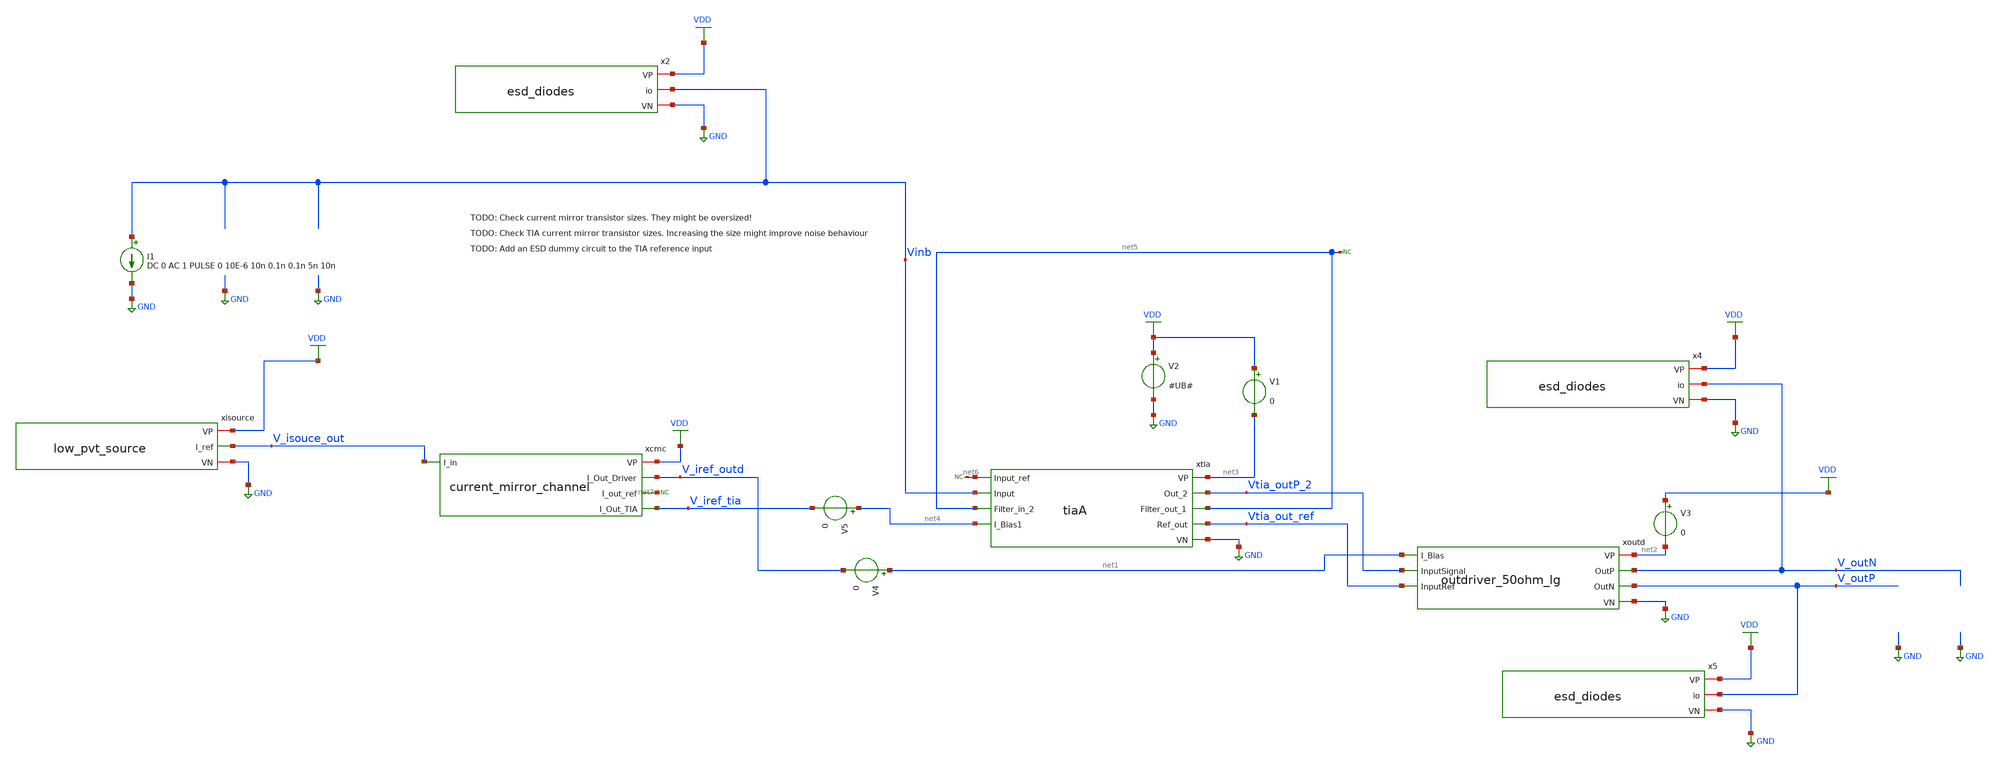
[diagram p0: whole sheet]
** sch_path: xschem/test/test_tia_integration_mc.sch
**.subckt test_tia_integration_mc
xisource VDD V_isouce_out GND low_pvt_source
I1 Vinb GND DC 0 AC 1 PULSE 0 10E-6 10n 0.1n 0.1n 5n 10n
xcmc VDD V_isouce_out V_iref_outd net7 V_iref_tia current_mirror_channel
x4 VDD V_outN GND esd_diodes
x5 VDD V_outP GND esd_diodes
x2 VDD Vinb GND esd_diodes
V2 VDD GND #UB#
V4 net1 V_iref_outd 0
V5 net4 V_iref_tia 0
V1 VDD net3 0
* noconn #net7
V3 VDD net2 0
xtia net3 Vtia_outP_2 net5 net6 Vinb net5 Vtia_out_ref net4 GND tiaA
* noconn #net5
* noconn #net6
xoutd net2 V_outN V_outP net1 Vtia_outP_2 Vtia_out_ref GND outdriver_50ohm_lg
**** begin user architecture code


*.options savecurrents
.option warn=1
* .option temp=100
.control
set wr_vecnames
set wr_singlescale
set hcopydevtype=svg
** TIA

set model="#model#"
let mc_runs=10
let mc_runNo = 1


dowhile mc_runNo <= mc_runs
   	destroy all
	let min_temp=0
	let var_temp = min_temp
	let max_temp=100
	let temp_step=30
	let noise_no=1
	dowhile var_temp <= max_temp
		option temp=$&var_temp
		save all
		op
 		wrdata 'result_op_op_{$&var_temp}deg_{$&mc_runNo}.csv' v(v_outp) v(v_outn) v(Vtia_outP_2) v(Vtia_out_ref)
+ v(v_outp)-v(v_outn)  i(V1) v(V_iref_outd) i(V2) i(V3) i(V4) i(V5) v(vinb)
 		*wrdata 'result_op_detail_{$&var_temp}deg_{$&mc_runNo}.csv' v(xtia.vm24D)
		* v(xtia.vm28D)  v(xoutd.v_da2_P)  v(xoutd.v_da2_N)
		* v(xoutd.v_da2_P)-v(xoutd.v_da2_N) v(xoutd.v_da3_P) v(xoutd.v_da3_N)
		* v(xoutd.v_da3_P)-v(xoutd.v_da3_N) v(v_outp_r)-v(v_outn_r)
		* v(xoutd.v_da2_P) v(xoutd.vm18d)
			* i(v.xtia.v1) i(v.xtia.v2)
		* AC analysis
		save all
		ac dec 10 10 1T

		wrdata 'result_ac_ac_{$&var_temp}deg_{$&mc_runNo}.csv' v(vinb) vdb(Vtia_outP_2)  db(v(v_outp)-v(v_outn))
		wrdata 'result_ac_detail_{$&var_temp}deg_{$&mc_runNo}.csv' db((v(xoutd.V_da2_P)-v(xoutd.V_da2_N))/(v(Vtia_outP_2)-v(Vtia_out_ref)))
+ db((v(xoutd.V_da3_P)-v(xoutd.V_da3_N))/(v(xoutd.V_da2_P)-v(xoutd.V_da2_N)))

		let vout_db=db(v(v_outp)-v(v_outn))
		*let vout_r_db=db(v(v_outp_r)-v(v_outn_r))
		*let dvout=v(v_outp)-v(v_outn)
		* Measure AC at output driver
		meas ac gain_tia FIND vdb(vtia_outp_2) AT=200MEG
		meas ac max_gain_tia max vdb(vtia_outp_2) from=1MEG to=100G
		meas ac min_gain_tia min vdb(vtia_outp_2) from=1MEG to=100MEG
		meas ac min_vinb min v(vinb) from=1MEG to=100G
		let bw_gain_tia=gain_tia-3
		meas ac bandwidth_tia when vdb(vtia_outp_2)=bw_gain_tia fall = LAST
		wrdata result_meas_tia_{$&var_temp}deg_{$&mc_runNo}.csv gain_tia max_gain_tia min_gain_tia bandwidth_tia
+ min_vinb


		* Measure AC at output driver
		meas ac gain_out FIND vout_db AT=10MEG
		meas ac max_gain_out max vout_db from=1MEG to=100G
		*meas ac max_gain_out max vout_db from=1MEG to=100G
		meas ac min_gain_out min vout_db from=1MEG to=100MEG
		*meas ac min_gain_out min vout_db from=1MEG to=100MEG
		let bw_gain_out=gain_out-3
		*let bw_gain_out_n=gain_out_n-3
		meas ac bandwidth_out when vout_db=bw_gain_out fall = LAST
		*meas ac bandwidth_out_r when vout_r_db=bw_gain_out fall = LAST
		*meas ac bandwidth_out_n when vout_db=bw_gain_out_n fall = LAST
		wrdata result_meas_out_{$&var_temp}deg_{$&mc_runNo}.csv gain_out max_gain_out  min_gain_out bandwidth_out


		* noise at TIA
		noise v(vtia_outp_2, vtia_out_ref) i1 dec 10 10 2G
		setplot noise1
		wrdata result_noise_tiaov_{$&var_temp}deg_{$&mc_runNo}.csv inoise_spectrum onoise_spectrum

		noise v(vtia_outp_2, vtia_out_ref) i1 dec 10 1MEG 2G
		setplot noise3
		wrdata result_noise_tiazoom_{$&var_temp}deg_{$&mc_runNo}.csv inoise_spectrum onoise_spectrum

		noise v(v_outp, v_outn) i1 dec 10 10 2G
		setplot noise5
		wrdata result_noise_outov_{$&var_temp}deg_{$&mc_runNo}.csv inoise_spectrum onoise_spectrum

		noise v(v_outp, v_outn) i1 dec 10 1MEG 2G
		setplot noise7
		wrdata result_noise_outzoom_{$&var_temp}deg_{$&mc_runNo}.csv inoise_spectrum onoise_spectrum

		tran 0.1ns 30ns

		wrdata result_tran_tran_{$&var_temp}deg_{$&mc_runNo}.csv v(Vtia_outP_2) v(v_outp)-v(v_outn)

		run
		let var_temp = var_temp + temp_step

	end
	let  mc_runNo = mc_runNo +1
	reset
end



.endc




* .include ../../tia.spice
* .include ../../filter_diff.spice
* .include ../../cmm_sense3.spice

.include tiaA.spice
.include current_mirror_channel.spice
.include low_pvt_source.spice
.include outdriver_50ohm_lg.spice
.include esd_diodes.spice



.lib $::SKYWATER_MODELS/sky130.lib.spice #model#
* .lib $::SKYWATER_MODELS/sky130.lib.spice sf
* .lib $::SKYWATER_MODELS/sky130.lib.spice.ll.red ll

**** end user architecture code
**.ends

* expanding   symbol:  ../bias/low_pvt_source.sym # of pins=3
** sym_path: ../bias/low_pvt_source.sym
** sch_path: ../bias/low_pvt_source.sch
.subckt low_pvt_source VP I_ref VN
*.iopin VP
*.opin I_ref
*.iopin VN
XM1 VM1D VM8D VP VP sky130_fd_pr__pfet_01v8 L=1 W=4 nf=1 ad='int((nf+1)/2) * W/nf * 0.29' as='int((nf+2)/2) * W/nf * 0.29'
+ pd='2*int((nf+1)/2) * (W/nf + 0.29)' ps='2*int((nf+2)/2) * (W/nf + 0.29)' nrd='0.29 / W' nrs='0.29 / W'
+ sa=0 sb=0 sd=0 mult=10 m=10
XM2 VM2D VM2D VN VN sky130_fd_pr__nfet_01v8 L=6 W=4 nf=1 ad='int((nf+1)/2) * W/nf * 0.29' as='int((nf+2)/2) * W/nf * 0.29'
+ pd='2*int((nf+1)/2) * (W/nf + 0.29)' ps='2*int((nf+2)/2) * (W/nf + 0.29)' nrd='0.29 / W' nrs='0.29 / W'
+ sa=0 sb=0 sd=0 mult=30 m=30
XM5 VM9D VM8D VM1D VP sky130_fd_pr__pfet_01v8 L=0.2 W=4 nf=1 ad='int((nf+1)/2) * W/nf * 0.29' as='int((nf+2)/2) * W/nf * 0.29'
+ pd='2*int((nf+1)/2) * (W/nf + 0.29)' ps='2*int((nf+2)/2) * (W/nf + 0.29)' nrd='0.29 / W' nrs='0.29 / W'
+ sa=0 sb=0 sd=0 mult=2 m=2
XM11 VM11D VM2D VM12D VN sky130_fd_pr__nfet_01v8 L=6 W=4 nf=1 ad='int((nf+1)/2) * W/nf * 0.29' as='int((nf+2)/2) * W/nf * 0.29'
+ pd='2*int((nf+1)/2) * (W/nf + 0.29)' ps='2*int((nf+2)/2) * (W/nf + 0.29)' nrd='0.29 / W' nrs='0.29 / W'
+ sa=0 sb=0 sd=0 mult=65 m=65
XM12 VM12D VM12G VN VN sky130_fd_pr__nfet_01v8 L=6 W=4 nf=1 ad='int((nf+1)/2) * W/nf * 0.29' as='int((nf+2)/2) * W/nf * 0.29'
+ pd='2*int((nf+1)/2) * (W/nf + 0.29)' ps='2*int((nf+2)/2) * (W/nf + 0.29)' nrd='0.29 / W' nrs='0.29 / W'
+ sa=0 sb=0 sd=0 mult=2 m=2
XM14 VM14D VM12G VN VN sky130_fd_pr__nfet_01v8 L=6 W=4 nf=1 ad='int((nf+1)/2) * W/nf * 0.29' as='int((nf+2)/2) * W/nf * 0.29'
+ pd='2*int((nf+1)/2) * (W/nf + 0.29)' ps='2*int((nf+2)/2) * (W/nf + 0.29)' nrd='0.29 / W' nrs='0.29 / W'
+ sa=0 sb=0 sd=0 mult=2 m=2
XM16 VM16D VM8D VP VP sky130_fd_pr__pfet_01v8 L=1 W=4 nf=1 ad='int((nf+1)/2) * W/nf * 0.29' as='int((nf+2)/2) * W/nf * 0.29'
+ pd='2*int((nf+1)/2) * (W/nf + 0.29)' ps='2*int((nf+2)/2) * (W/nf + 0.29)' nrd='0.29 / W' nrs='0.29 / W'
+ sa=0 sb=0 sd=0 mult=10 m=10
XM17 VM8D VM8D VM16D VP sky130_fd_pr__pfet_01v8 L=0.2 W=4 nf=1 ad='int((nf+1)/2) * W/nf * 0.29' as='int((nf+2)/2) * W/nf * 0.29'
+ pd='2*int((nf+1)/2) * (W/nf + 0.29)' ps='2*int((nf+2)/2) * (W/nf + 0.29)' nrd='0.29 / W' nrs='0.29 / W'
+ sa=0 sb=0 sd=0 mult=2 m=2
XM18 VM18D VM8D VP VP sky130_fd_pr__pfet_01v8 L=1 W=4 nf=1 ad='int((nf+1)/2) * W/nf * 0.29' as='int((nf+2)/2) * W/nf * 0.29'
+ pd='2*int((nf+1)/2) * (W/nf + 0.29)' ps='2*int((nf+2)/2) * (W/nf + 0.29)' nrd='0.29 / W' nrs='0.29 / W'
+ sa=0 sb=0 sd=0 mult=10*3*2 m=10*3*2
XM19 VM14D VM8D VM18D VP sky130_fd_pr__pfet_01v8 L=0.2 W=4 nf=1 ad='int((nf+1)/2) * W/nf * 0.29' as='int((nf+2)/2) * W/nf * 0.29'
+ pd='2*int((nf+1)/2) * (W/nf + 0.29)' ps='2*int((nf+2)/2) * (W/nf + 0.29)' nrd='0.29 / W' nrs='0.29 / W'
+ sa=0 sb=0 sd=0 mult=2*3*2 m=2*3*2
XM20 VM20D VM8D VP VP sky130_fd_pr__pfet_01v8 L=1 W=4 nf=1 ad='int((nf+1)/2) * W/nf * 0.29' as='int((nf+2)/2) * W/nf * 0.29'
+ pd='2*int((nf+1)/2) * (W/nf + 0.29)' ps='2*int((nf+2)/2) * (W/nf + 0.29)' nrd='0.29 / W' nrs='0.29 / W'
+ sa=0 sb=0 sd=0 mult=10*1*1 m=10*1*1
XM21 VM22D VM8D VM20D VP sky130_fd_pr__pfet_01v8 L=0.2 W=4 nf=1 ad='int((nf+1)/2) * W/nf * 0.29' as='int((nf+2)/2) * W/nf * 0.29'
+ pd='2*int((nf+1)/2) * (W/nf + 0.29)' ps='2*int((nf+2)/2) * (W/nf + 0.29)' nrd='0.29 / W' nrs='0.29 / W'
+ sa=0 sb=0 sd=0 mult=2*1*1 m=2*1*1
XM22 VM22D VM4S VM3D VN sky130_fd_pr__nfet_01v8 L=6 W=4 nf=1 ad='int((nf+1)/2) * W/nf * 0.29' as='int((nf+2)/2) * W/nf * 0.29'
+ pd='2*int((nf+1)/2) * (W/nf + 0.29)' ps='2*int((nf+2)/2) * (W/nf + 0.29)' nrd='0.29 / W' nrs='0.29 / W'
+ sa=0 sb=0 sd=0 mult=20 m=20
XM3 VM3D VM3G VN VN sky130_fd_pr__nfet_01v8 L=6 W=4 nf=1 ad='int((nf+1)/2) * W/nf * 0.29' as='int((nf+2)/2) * W/nf * 0.29'
+ pd='2*int((nf+1)/2) * (W/nf + 0.29)' ps='2*int((nf+2)/2) * (W/nf + 0.29)' nrd='0.29 / W' nrs='0.29 / W'
+ sa=0 sb=0 sd=0 mult=4 m=4
XM13 VP VM14D VM12G VM12G sky130_fd_pr__nfet_01v8_lvt L=0.15 W=4 nf=1 ad='int((nf+1)/2) * W/nf * 0.29'
+ as='int((nf+2)/2) * W/nf * 0.29' pd='2*int((nf+1)/2) * (W/nf + 0.29)' ps='2*int((nf+2)/2) * (W/nf + 0.29)'
+ nrd='0.29 / W' nrs='0.29 / W' sa=0 sb=0 sd=0 mult=20 m=20
XM4 I_ref VM22D VM4S VN sky130_fd_pr__nfet_01v8_lvt L=0.15 W=4 nf=1 ad='int((nf+1)/2) * W/nf * 0.29'
+ as='int((nf+2)/2) * W/nf * 0.29' pd='2*int((nf+1)/2) * (W/nf + 0.29)' ps='2*int((nf+2)/2) * (W/nf + 0.29)'
+ nrd='0.29 / W' nrs='0.29 / W' sa=0 sb=0 sd=0 mult=20 m=20
XM48 VM50D VM11D VP VP sky130_fd_pr__pfet_01v8 L=2 W=0.5 nf=1 ad='int((nf+1)/2) * W/nf * 0.29' as='int((nf+2)/2) * W/nf * 0.29'
+ pd='2*int((nf+1)/2) * (W/nf + 0.29)' ps='2*int((nf+2)/2) * (W/nf + 0.29)' nrd='0.29 / W' nrs='0.29 / W'
+ sa=0 sb=0 sd=0 mult=1 m=1
XM50 VM50D VM11D VN VN sky130_fd_pr__nfet_01v8_lvt L=0.2 W=4 nf=1 ad='int((nf+1)/2) * W/nf * 0.29' as='int((nf+2)/2) * W/nf * 0.29'
+ pd='2*int((nf+1)/2) * (W/nf + 0.29)' ps='2*int((nf+2)/2) * (W/nf + 0.29)' nrd='0.29 / W' nrs='0.29 / W'
+ sa=0 sb=0 sd=0 mult=10 m=10
XC3 VP VM8D sky130_fd_pr__cap_mim_m3_1 W=20 L=20 MF=1 m=1
XM8 VM8D VM9D VM11D VM11D sky130_fd_pr__nfet_01v8_lvt L=1 W=4 nf=1 ad='int((nf+1)/2) * W/nf * 0.29' as='int((nf+2)/2) * W/nf * 0.29'
+ pd='2*int((nf+1)/2) * (W/nf + 0.29)' ps='2*int((nf+2)/2) * (W/nf + 0.29)' nrd='0.29 / W' nrs='0.29 / W'
+ sa=0 sb=0 sd=0 mult=20 m=20
XM9 VM9D VM9D VM2D VM2D sky130_fd_pr__nfet_01v8_lvt L=1 W=4 nf=1 ad='int((nf+1)/2) * W/nf * 0.29' as='int((nf+2)/2) * W/nf * 0.29'
+ pd='2*int((nf+1)/2) * (W/nf + 0.29)' ps='2*int((nf+2)/2) * (W/nf + 0.29)' nrd='0.29 / W' nrs='0.29 / W'
+ sa=0 sb=0 sd=0 mult=20 m=20
XM10 VM8D VM50D VN VN sky130_fd_pr__nfet_01v8 L=2 W=0.5 nf=1 ad='int((nf+1)/2) * W/nf * 0.29' as='int((nf+2)/2) * W/nf * 0.29'
+ pd='2*int((nf+1)/2) * (W/nf + 0.29)' ps='2*int((nf+2)/2) * (W/nf + 0.29)' nrd='0.29 / W' nrs='0.29 / W'
+ sa=0 sb=0 sd=0 mult=1 m=1
XR7 net3 VM4S VN sky130_fd_pr__res_xhigh_po_1p41 L=10 mult=1 m=1
XR3 net4 net3 VN sky130_fd_pr__res_xhigh_po_1p41 L=10 mult=1 m=1
XR4 net2 net4 VN sky130_fd_pr__res_xhigh_po_1p41 L=10 mult=1 m=1
XR5 net1 net2 VN sky130_fd_pr__res_xhigh_po_1p41 L=10 mult=1 m=1
XR6 VN net1 VN sky130_fd_pr__res_xhigh_po_1p41 L=10 mult=1 m=1
XR8 net5 VM12G VN sky130_fd_pr__res_xhigh_po_1p41 L=10 mult=1 m=1
XR1 net5 VM3G VN sky130_fd_pr__res_xhigh_po_1p41 L=10 mult=1 m=1
XR2 net7 net6 VN sky130_fd_pr__res_xhigh_po_1p41 L=10 mult=1 m=1
XR9 VN net6 VN sky130_fd_pr__res_xhigh_po_1p41 L=10 mult=1 m=1
XR10 net11 net7 VN sky130_fd_pr__res_xhigh_po_1p41 L=10 mult=1 m=1
XR11 net12 net11 VN sky130_fd_pr__res_xhigh_po_1p41 L=10 mult=1 m=1
XR12 net8 net12 VN sky130_fd_pr__res_xhigh_po_1p41 L=10 mult=1 m=1
XR13 net10 VM3G VN sky130_fd_pr__res_xhigh_po_1p41 L=10 mult=1 m=1
XR14 net9 net10 VN sky130_fd_pr__res_xhigh_po_1p41 L=10 mult=1 m=1
XR15 net8 net9 VN sky130_fd_pr__res_xhigh_po_1p41 L=10 mult=1 m=1
XC2 VP VN sky130_fd_pr__cap_mim_m3_1 W=25 L=30 MF=1 m=1
XC1 VP VN sky130_fd_pr__cap_mim_m3_1 W=25 L=30 MF=1 m=1
.ends


* expanding   symbol:  ../bias/current_mirror_channel.sym # of pins=5
** sym_path: xschem/bias/current_mirror_channel.sym
** sch_path: xschem/bias/current_mirror_channel.sch
.subckt current_mirror_channel VP I_in I_Out_Driver I_out_ref I_Out_TIA
*.ipin I_in
*.iopin VP
*.opin I_Out_TIA
*.opin I_Out_Driver
*.opin I_out_ref
XM13 VM13D I_in VP VP sky130_fd_pr__pfet_01v8 L=1 W=2 nf=1 ad='int((nf+1)/2) * W/nf * 0.29' as='int((nf+2)/2) * W/nf * 0.29'
+ pd='2*int((nf+1)/2) * (W/nf + 0.29)' ps='2*int((nf+2)/2) * (W/nf + 0.29)' nrd='0.29 / W' nrs='0.29 / W'
+ sa=0 sb=0 sd=0 mult=8*16 m=8*16
XM11 VM11D I_in VP VP sky130_fd_pr__pfet_01v8 L=1 W=2 nf=1 ad='int((nf+1)/2) * W/nf * 0.29' as='int((nf+2)/2) * W/nf * 0.29'
+ pd='2*int((nf+1)/2) * (W/nf + 0.29)' ps='2*int((nf+2)/2) * (W/nf + 0.29)' nrd='0.29 / W' nrs='0.29 / W'
+ sa=0 sb=0 sd=0 mult=16 m=16
XM2 I_in I_in VM11D VP sky130_fd_pr__pfet_01v8 L=0.15 W=2 nf=1 ad='int((nf+1)/2) * W/nf * 0.29' as='int((nf+2)/2) * W/nf * 0.29'
+ pd='2*int((nf+1)/2) * (W/nf + 0.29)' ps='2*int((nf+2)/2) * (W/nf + 0.29)' nrd='0.29 / W' nrs='0.29 / W'
+ sa=0 sb=0 sd=0 mult=16 m=16
XM4 I_Out_TIA I_in VM13D VP sky130_fd_pr__pfet_01v8 L=0.15 W=2 nf=1 ad='int((nf+1)/2) * W/nf * 0.29'
+ as='int((nf+2)/2) * W/nf * 0.29' pd='2*int((nf+1)/2) * (W/nf + 0.29)' ps='2*int((nf+2)/2) * (W/nf + 0.29)'
+ nrd='0.29 / W' nrs='0.29 / W' sa=0 sb=0 sd=0 mult=8*16 m=8*16
XM1 VM1D I_in VP VP sky130_fd_pr__pfet_01v8 L=1 W=2 nf=1 ad='int((nf+1)/2) * W/nf * 0.29' as='int((nf+2)/2) * W/nf * 0.29'
+ pd='2*int((nf+1)/2) * (W/nf + 0.29)' ps='2*int((nf+2)/2) * (W/nf + 0.29)' nrd='0.29 / W' nrs='0.29 / W'
+ sa=0 sb=0 sd=0 mult=2*2*8*16 m=2*2*8*16
XM3 I_Out_Driver I_in VM1D VP sky130_fd_pr__pfet_01v8 L=0.15 W=2 nf=1 ad='int((nf+1)/2) * W/nf * 0.29'
+ as='int((nf+2)/2) * W/nf * 0.29' pd='2*int((nf+1)/2) * (W/nf + 0.29)' ps='2*int((nf+2)/2) * (W/nf + 0.29)'
+ nrd='0.29 / W' nrs='0.29 / W' sa=0 sb=0 sd=0 mult=2*2*8*16 m=2*2*8*16
XM5 VM5D I_in VP VP sky130_fd_pr__pfet_01v8 L=1 W=2 nf=1 ad='int((nf+1)/2) * W/nf * 0.29' as='int((nf+2)/2) * W/nf * 0.29'
+ pd='2*int((nf+1)/2) * (W/nf + 0.29)' ps='2*int((nf+2)/2) * (W/nf + 0.29)' nrd='0.29 / W' nrs='0.29 / W'
+ sa=0 sb=0 sd=0 mult=8*16 m=8*16
XM6 I_out_ref I_in VM5D VP sky130_fd_pr__pfet_01v8 L=0.15 W=2 nf=1 ad='int((nf+1)/2) * W/nf * 0.29' as='int((nf+2)/2) * W/nf * 0.29'
+ pd='2*int((nf+1)/2) * (W/nf + 0.29)' ps='2*int((nf+2)/2) * (W/nf + 0.29)' nrd='0.29 / W' nrs='0.29 / W'
+ sa=0 sb=0 sd=0 mult=8*16 m=8*16
.ends


* expanding   symbol:  ../esd/esd_diodes.sym # of pins=3
** sym_path: ../esd/esd_diodes.sym
** sch_path: ../esd/esd_diodes.sch
.subckt esd_diodes VP io VN
*.iopin VP
*.iopin io
*.iopin VN
XD1 io VP sky130_fd_pr__diode_pw2nd_05v5 area=4e12 pj=4e6
XD2 io VP sky130_fd_pr__diode_pw2nd_05v5 area=4e12 pj=4e6
XD3 io VP sky130_fd_pr__diode_pw2nd_05v5 area=4e12 pj=4e6
XD4 io VP sky130_fd_pr__diode_pw2nd_05v5 area=4e12 pj=4e6
XD5 io VP sky130_fd_pr__diode_pw2nd_05v5 area=4e12 pj=4e6
XD6 io VP sky130_fd_pr__diode_pw2nd_05v5 area=4e12 pj=4e6
XD7 io VP sky130_fd_pr__diode_pw2nd_05v5 area=4e12 pj=4e6
XD8 io VP sky130_fd_pr__diode_pw2nd_05v5 area=4e12 pj=4e6
XD9 io VP sky130_fd_pr__diode_pw2nd_05v5 area=4e12 pj=4e6
XD10 io VP sky130_fd_pr__diode_pw2nd_05v5 area=4e12 pj=4e6
XD11 VN io sky130_fd_pr__diode_pw2nd_05v5 area=4e12 pj=4e6
XD12 VN io sky130_fd_pr__diode_pw2nd_05v5 area=4e12 pj=4e6
XD13 VN io sky130_fd_pr__diode_pw2nd_05v5 area=4e12 pj=4e6
XD14 VN io sky130_fd_pr__diode_pw2nd_05v5 area=4e12 pj=4e6
XD15 VN io sky130_fd_pr__diode_pw2nd_05v5 area=4e12 pj=4e6
XD16 VN io sky130_fd_pr__diode_pw2nd_05v5 area=4e12 pj=4e6
XD17 VN io sky130_fd_pr__diode_pw2nd_05v5 area=4e12 pj=4e6
XD18 VN io sky130_fd_pr__diode_pw2nd_05v5 area=4e12 pj=4e6
XD19 VN io sky130_fd_pr__diode_pw2nd_05v5 area=4e12 pj=4e6
XD20 VN io sky130_fd_pr__diode_pw2nd_05v5 area=4e12 pj=4e6
.ends


* expanding   symbol:  /home/simon/code/hibpm-sky130a-tapeout/xschem/tia/tiaA.sym # of pins=9
** sym_path: xschem/tia/tiaA.sym
** sch_path: xschem/tia/tiaA.sch
.subckt tiaA VP Out_2 Filter_out_1 Input_ref Input Filter_in_2 Ref_out I_Bias1 VN
*.iopin VN
*.iopin VP
*.opin Out_2
*.ipin I_Bias1
*.ipin Input
*.ipin Input_ref
*.opin Filter_out_1
*.ipin Filter_in_2
*.opin Ref_out
XM7 VM7D Input VN VN sky130_fd_pr__nfet_01v8_lvt L=0.15 W=2 nf=1 ad='int((nf+1)/2) * W/nf * 0.29' as='int((nf+2)/2) * W/nf * 0.29'
+ pd='2*int((nf+1)/2) * (W/nf + 0.29)' ps='2*int((nf+2)/2) * (W/nf + 0.29)' nrd='0.29 / W' nrs='0.29 / W'
+ sa=0 sb=0 sd=0 mult=180 m=180
XM8 net1 Input VP VP sky130_fd_pr__pfet_01v8 L=0.15 W=2 nf=1 ad='int((nf+1)/2) * W/nf * 0.29' as='int((nf+2)/2) * W/nf * 0.29'
+ pd='2*int((nf+1)/2) * (W/nf + 0.29)' ps='2*int((nf+2)/2) * (W/nf + 0.29)' nrd='0.29 / W' nrs='0.29 / W'
+ sa=0 sb=0 sd=0 mult=40 m=40
XC4 VN VM9G sky130_fd_pr__cap_mim_m3_1 W=15 L=20 MF=1 m=1
XM18 I_Bias1 I_Bias1 VM10G VN sky130_fd_pr__nfet_01v8_lvt L=0.15 W=2 nf=1 ad='int((nf+1)/2) * W/nf * 0.29'
+ as='int((nf+2)/2) * W/nf * 0.29' pd='2*int((nf+1)/2) * (W/nf + 0.29)' ps='2*int((nf+2)/2) * (W/nf + 0.29)'
+ nrd='0.29 / W' nrs='0.29 / W' sa=0 sb=0 sd=0 mult=30 m=30
XM10 VM10G VM10G VM6D VN sky130_fd_pr__nfet_01v8_lvt L=0.15 W=2 nf=1 ad='int((nf+1)/2) * W/nf * 0.29'
+ as='int((nf+2)/2) * W/nf * 0.29' pd='2*int((nf+1)/2) * (W/nf + 0.29)' ps='2*int((nf+2)/2) * (W/nf + 0.29)'
+ nrd='0.29 / W' nrs='0.29 / W' sa=0 sb=0 sd=0 mult=30 m=30
XM5 Input VM9G VM5D VN sky130_fd_pr__nfet_01v8_lvt L=0.15 W=2 nf=1 ad='int((nf+1)/2) * W/nf * 0.29' as='int((nf+2)/2) * W/nf * 0.29'
+ pd='2*int((nf+1)/2) * (W/nf + 0.29)' ps='2*int((nf+2)/2) * (W/nf + 0.29)' nrd='0.29 / W' nrs='0.29 / W'
+ sa=0 sb=0 sd=0 mult=120 m=120
XM6 VM6D VM10G VN VN sky130_fd_pr__nfet_01v8_lvt L=1 W=2 nf=1 ad='int((nf+1)/2) * W/nf * 0.29' as='int((nf+2)/2) * W/nf * 0.29'
+ pd='2*int((nf+1)/2) * (W/nf + 0.29)' ps='2*int((nf+2)/2) * (W/nf + 0.29)' nrd='0.29 / W' nrs='0.29 / W'
+ sa=0 sb=0 sd=0 mult=30 m=30
XM14 VM9G I_Bias1 VM10G VN sky130_fd_pr__nfet_01v8_lvt L=8 W=1 nf=1 ad='int((nf+1)/2) * W/nf * 0.29'
+ as='int((nf+2)/2) * W/nf * 0.29' pd='2*int((nf+1)/2) * (W/nf + 0.29)' ps='2*int((nf+2)/2) * (W/nf + 0.29)'
+ nrd='0.29 / W' nrs='0.29 / W' sa=0 sb=0 sd=0 mult=1 m=1
XM1 Out_2 net1 Input Input sky130_fd_pr__nfet_01v8_lvt L=0.15 W=2 nf=1 ad='int((nf+1)/2) * W/nf * 0.29'
+ as='int((nf+2)/2) * W/nf * 0.29' pd='2*int((nf+1)/2) * (W/nf + 0.29)' ps='2*int((nf+2)/2) * (W/nf + 0.29)'
+ nrd='0.29 / W' nrs='0.29 / W' sa=0 sb=0 sd=0 mult=60 m=60
XM3 VM5D VM9G VN VN sky130_fd_pr__nfet_01v8_lvt L=1 W=2 nf=1 ad='int((nf+1)/2) * W/nf * 0.29' as='int((nf+2)/2) * W/nf * 0.29'
+ pd='2*int((nf+1)/2) * (W/nf + 0.29)' ps='2*int((nf+2)/2) * (W/nf + 0.29)' nrd='0.29 / W' nrs='0.29 / W'
+ sa=0 sb=0 sd=0 mult=120 m=120
XR1 Out_2 VP VN sky130_fd_pr__res_xhigh_po_1p41 L=4 mult=6 m=6
XM2 VM2D Input_ref VN VN sky130_fd_pr__nfet_01v8_lvt L=0.15 W=2 nf=1 ad='int((nf+1)/2) * W/nf * 0.29'
+ as='int((nf+2)/2) * W/nf * 0.29' pd='2*int((nf+1)/2) * (W/nf + 0.29)' ps='2*int((nf+2)/2) * (W/nf + 0.29)'
+ nrd='0.29 / W' nrs='0.29 / W' sa=0 sb=0 sd=0 mult=180 m=180
XM4 net3 Input_ref VP VP sky130_fd_pr__pfet_01v8 L=0.15 W=2 nf=1 ad='int((nf+1)/2) * W/nf * 0.29' as='int((nf+2)/2) * W/nf * 0.29'
+ pd='2*int((nf+1)/2) * (W/nf + 0.29)' ps='2*int((nf+2)/2) * (W/nf + 0.29)' nrd='0.29 / W' nrs='0.29 / W'
+ sa=0 sb=0 sd=0 mult=40 m=40
XM11 Input_ref VM9G VM15D VN sky130_fd_pr__nfet_01v8_lvt L=0.15 W=2 nf=1 ad='int((nf+1)/2) * W/nf * 0.29'
+ as='int((nf+2)/2) * W/nf * 0.29' pd='2*int((nf+1)/2) * (W/nf + 0.29)' ps='2*int((nf+2)/2) * (W/nf + 0.29)'
+ nrd='0.29 / W' nrs='0.29 / W' sa=0 sb=0 sd=0 mult=120 m=120
XM12 net2 net3 Input_ref Input_ref sky130_fd_pr__nfet_01v8_lvt L=0.15 W=2 nf=1 ad='int((nf+1)/2) * W/nf * 0.29'
+ as='int((nf+2)/2) * W/nf * 0.29' pd='2*int((nf+1)/2) * (W/nf + 0.29)' ps='2*int((nf+2)/2) * (W/nf + 0.29)'
+ nrd='0.29 / W' nrs='0.29 / W' sa=0 sb=0 sd=0 mult=60 m=60
XM15 VM15D VM9G VN VN sky130_fd_pr__nfet_01v8_lvt L=1 W=2 nf=1 ad='int((nf+1)/2) * W/nf * 0.29' as='int((nf+2)/2) * W/nf * 0.29'
+ pd='2*int((nf+1)/2) * (W/nf + 0.29)' ps='2*int((nf+2)/2) * (W/nf + 0.29)' nrd='0.29 / W' nrs='0.29 / W'
+ sa=0 sb=0 sd=0 mult=120 m=120
XR2 net2 VP VN sky130_fd_pr__res_xhigh_po_1p41 L=4 mult=6 m=6
XC5 VN VP sky130_fd_pr__cap_mim_m3_1 W=15 L=30 MF=1 m=1
XC1 VN VP sky130_fd_pr__cap_mim_m3_1 W=15 L=30 MF=1 m=1
XC2 VN Filter_out_1 sky130_fd_pr__cap_mim_m3_1 W=30 L=10 MF=1 m=1
XM29 VM29D VM9G VM33D VN sky130_fd_pr__nfet_01v8_lvt L=0.15 W=2 nf=1 ad='int((nf+1)/2) * W/nf * 0.29'
+ as='int((nf+2)/2) * W/nf * 0.29' pd='2*int((nf+1)/2) * (W/nf + 0.29)' ps='2*int((nf+2)/2) * (W/nf + 0.29)'
+ nrd='0.29 / W' nrs='0.29 / W' sa=0 sb=0 sd=0 mult=20 m=20
XM33 VM33D VM9G VN VN sky130_fd_pr__nfet_01v8_lvt L=1 W=2 nf=1 ad='int((nf+1)/2) * W/nf * 0.29' as='int((nf+2)/2) * W/nf * 0.29'
+ pd='2*int((nf+1)/2) * (W/nf + 0.29)' ps='2*int((nf+2)/2) * (W/nf + 0.29)' nrd='0.29 / W' nrs='0.29 / W'
+ sa=0 sb=0 sd=0 mult=20 m=20
XR3 VM21D VP VN sky130_fd_pr__res_xhigh_po_1p41 L=4 mult=1 m=1
XM21 VM29D VM29D VM21D VP sky130_fd_pr__pfet_01v8 L=0.15 W=2 nf=1 ad='int((nf+1)/2) * W/nf * 0.29' as='int((nf+2)/2) * W/nf * 0.29'
+ pd='2*int((nf+1)/2) * (W/nf + 0.29)' ps='2*int((nf+2)/2) * (W/nf + 0.29)' nrd='0.29 / W' nrs='0.29 / W'
+ sa=0 sb=0 sd=0 mult=10 m=10
XM13 Filter_out_1 VM29D net2 VP sky130_fd_pr__pfet_01v8 L=8 W=1 nf=1 ad='int((nf+1)/2) * W/nf * 0.29'
+ as='int((nf+2)/2) * W/nf * 0.29' pd='2*int((nf+1)/2) * (W/nf + 0.29)' ps='2*int((nf+2)/2) * (W/nf + 0.29)'
+ nrd='0.29 / W' nrs='0.29 / W' sa=0 sb=0 sd=0 mult=1 m=1
XM24 VM24D Input_ref VN VN sky130_fd_pr__nfet_01v8_lvt L=0.15 W=2 nf=1 ad='int((nf+1)/2) * W/nf * 0.29'
+ as='int((nf+2)/2) * W/nf * 0.29' pd='2*int((nf+1)/2) * (W/nf + 0.29)' ps='2*int((nf+2)/2) * (W/nf + 0.29)'
+ nrd='0.29 / W' nrs='0.29 / W' sa=0 sb=0 sd=0 mult=20 m=20
XM30 VM30D VM9G VM31D VN sky130_fd_pr__nfet_01v8_lvt L=0.15 W=2 nf=1 ad='int((nf+1)/2) * W/nf * 0.29'
+ as='int((nf+2)/2) * W/nf * 0.29' pd='2*int((nf+1)/2) * (W/nf + 0.29)' ps='2*int((nf+2)/2) * (W/nf + 0.29)'
+ nrd='0.29 / W' nrs='0.29 / W' sa=0 sb=0 sd=0 mult=2*30 m=2*30
XM31 VM31D VM9G VN VN sky130_fd_pr__nfet_01v8_lvt L=1 W=2 nf=1 ad='int((nf+1)/2) * W/nf * 0.29' as='int((nf+2)/2) * W/nf * 0.29'
+ pd='2*int((nf+1)/2) * (W/nf + 0.29)' ps='2*int((nf+2)/2) * (W/nf + 0.29)' nrd='0.29 / W' nrs='0.29 / W'
+ sa=0 sb=0 sd=0 mult=2*30 m=2*30
XM28 VM28D VM28D VM24D VN sky130_fd_pr__nfet_01v8_lvt L=0.15 W=2 nf=1 ad='int((nf+1)/2) * W/nf * 0.29'
+ as='int((nf+2)/2) * W/nf * 0.29' pd='2*int((nf+1)/2) * (W/nf + 0.29)' ps='2*int((nf+2)/2) * (W/nf + 0.29)'
+ nrd='0.29 / W' nrs='0.29 / W' sa=0 sb=0 sd=0 mult=7 m=7
XM17 net1 VM28D VM7D VN sky130_fd_pr__nfet_01v8_lvt L=0.15 W=2 nf=1 ad='int((nf+1)/2) * W/nf * 0.29'
+ as='int((nf+2)/2) * W/nf * 0.29' pd='2*int((nf+1)/2) * (W/nf + 0.29)' ps='2*int((nf+2)/2) * (W/nf + 0.29)'
+ nrd='0.29 / W' nrs='0.29 / W' sa=0 sb=0 sd=0 mult=40 m=40
XM9 net3 VM28D VM2D VN sky130_fd_pr__nfet_01v8_lvt L=0.15 W=2 nf=1 ad='int((nf+1)/2) * W/nf * 0.29' as='int((nf+2)/2) * W/nf * 0.29'
+ pd='2*int((nf+1)/2) * (W/nf + 0.29)' ps='2*int((nf+2)/2) * (W/nf + 0.29)' nrd='0.29 / W' nrs='0.29 / W'
+ sa=0 sb=0 sd=0 mult=40 m=40
XC10 VN VM28D sky130_fd_pr__cap_mim_m3_1 W=25 L=10 MF=1 m=1
XC11 VN VM28D sky130_fd_pr__cap_mim_m3_1 W=25 L=10 MF=1 m=1
XM36 VM36D VM30D VP VP sky130_fd_pr__pfet_01v8 L=0.5 W=2 nf=1 ad='int((nf+1)/2) * W/nf * 0.29' as='int((nf+2)/2) * W/nf * 0.29'
+ pd='2*int((nf+1)/2) * (W/nf + 0.29)' ps='2*int((nf+2)/2) * (W/nf + 0.29)' nrd='0.29 / W' nrs='0.29 / W'
+ sa=0 sb=0 sd=0 mult=1*30 m=1*30
XM16 VM16D VM30D VP VP sky130_fd_pr__pfet_01v8 L=0.5 W=2 nf=1 ad='int((nf+1)/2) * W/nf * 0.29' as='int((nf+2)/2) * W/nf * 0.29'
+ pd='2*int((nf+1)/2) * (W/nf + 0.29)' ps='2*int((nf+2)/2) * (W/nf + 0.29)' nrd='0.29 / W' nrs='0.29 / W'
+ sa=0 sb=0 sd=0 mult=4*30 m=4*30
XM19 VM28D VM30D VM16D VP sky130_fd_pr__pfet_01v8 L=0.15 W=2 nf=1 ad='int((nf+1)/2) * W/nf * 0.29' as='int((nf+2)/2) * W/nf * 0.29'
+ pd='2*int((nf+1)/2) * (W/nf + 0.29)' ps='2*int((nf+2)/2) * (W/nf + 0.29)' nrd='0.29 / W' nrs='0.29 / W'
+ sa=0 sb=0 sd=0 mult=4*30 m=4*30
XM20 VM30D VM30D VM36D VP sky130_fd_pr__pfet_01v8 L=0.15 W=2 nf=1 ad='int((nf+1)/2) * W/nf * 0.29' as='int((nf+2)/2) * W/nf * 0.29'
+ pd='2*int((nf+1)/2) * (W/nf + 0.29)' ps='2*int((nf+2)/2) * (W/nf + 0.29)' nrd='0.29 / W' nrs='0.29 / W'
+ sa=0 sb=0 sd=0 mult=1*30 m=1*30
XC8 VN Ref_out sky130_fd_pr__cap_mim_m3_1 W=5 L=2 MF=1 m=1
XR9 Ref_out Filter_in_2 VN sky130_fd_pr__res_xhigh_po_0p69 L=6 mult=1 m=1
XC3 VN VM9G sky130_fd_pr__cap_mim_m3_1 W=15 L=20 MF=1 m=1
.ends


* expanding   symbol:
*+  /home/simon/code/hibpm-sky130a-tapeout/xschem/outdriver/outdriver_50ohm_lg.sym # of pins=7
** sym_path: xschem/outdriver/outdriver_50ohm_lg.sym
** sch_path: xschem/outdriver/outdriver_50ohm_lg.sch
.subckt outdriver_50ohm_lg VP OutP OutN I_Bias InputSignal InputRef VN
*.iopin VN
*.ipin InputRef
*.iopin VP
*.ipin I_Bias
*.ipin InputSignal
*.opin OutN
*.opin OutP
XM17 net1 VM18D VN VN sky130_fd_pr__nfet_01v8_lvt L=0.3 W=2 nf=1 ad='int((nf+1)/2) * W/nf * 0.29' as='int((nf+2)/2) * W/nf * 0.29'
+ pd='2*int((nf+1)/2) * (W/nf + 0.29)' ps='2*int((nf+2)/2) * (W/nf + 0.29)' nrd='0.29 / W' nrs='0.29 / W'
+ sa=0 sb=0 sd=0 mult=6 m=6
XM18 VM18D VM18D net1 VN sky130_fd_pr__nfet_01v8_lvt L=0.15 W=2 nf=1 ad='int((nf+1)/2) * W/nf * 0.29'
+ as='int((nf+2)/2) * W/nf * 0.29' pd='2*int((nf+1)/2) * (W/nf + 0.29)' ps='2*int((nf+2)/2) * (W/nf + 0.29)'
+ nrd='0.29 / W' nrs='0.29 / W' sa=0 sb=0 sd=0 mult=12 m=12
XM7 I_Bias I_Bias VM18D VM18D sky130_fd_pr__nfet_01v8_lvt L=0.15 W=2 nf=1 ad='int((nf+1)/2) * W/nf * 0.29'
+ as='int((nf+2)/2) * W/nf * 0.29' pd='2*int((nf+1)/2) * (W/nf + 0.29)' ps='2*int((nf+2)/2) * (W/nf + 0.29)'
+ nrd='0.29 / W' nrs='0.29 / W' sa=0 sb=0 sd=0 mult=20 m=20
XM5 VM5D net2 net3 VN sky130_fd_pr__nfet_01v8_lvt L=0.15 W=2 nf=1 ad='int((nf+1)/2) * W/nf * 0.29' as='int((nf+2)/2) * W/nf * 0.29'
+ pd='2*int((nf+1)/2) * (W/nf + 0.29)' ps='2*int((nf+2)/2) * (W/nf + 0.29)' nrd='0.29 / W' nrs='0.29 / W'
+ sa=0 sb=0 sd=0 mult=12*5 m=12*5
XM8 net3 net2 VN VN sky130_fd_pr__nfet_01v8_lvt L=0.3 W=2 nf=1 ad='int((nf+1)/2) * W/nf * 0.29' as='int((nf+2)/2) * W/nf * 0.29'
+ pd='2*int((nf+1)/2) * (W/nf + 0.29)' ps='2*int((nf+2)/2) * (W/nf + 0.29)' nrd='0.29 / W' nrs='0.29 / W'
+ sa=0 sb=0 sd=0 mult=6*5 m=6*5
XM6 net2 I_Bias VM18D VM18D sky130_fd_pr__nfet_01v8_lvt L=8 W=1 nf=1 ad='int((nf+1)/2) * W/nf * 0.29'
+ as='int((nf+2)/2) * W/nf * 0.29' pd='2*int((nf+1)/2) * (W/nf + 0.29)' ps='2*int((nf+2)/2) * (W/nf + 0.29)'
+ nrd='0.29 / W' nrs='0.29 / W' sa=0 sb=0 sd=0 mult=1 m=1
XC1 VN VP sky130_fd_pr__cap_mim_m3_1 W=15 L=30 MF=1 m=1
XM15 VM15D net2 net4 VN sky130_fd_pr__nfet_01v8_lvt L=0.15 W=2 nf=1 ad='int((nf+1)/2) * W/nf * 0.29'
+ as='int((nf+2)/2) * W/nf * 0.29' pd='2*int((nf+1)/2) * (W/nf + 0.29)' ps='2*int((nf+2)/2) * (W/nf + 0.29)'
+ nrd='0.29 / W' nrs='0.29 / W' sa=0 sb=0 sd=0 mult=34*12 m=34*12
XM16 net4 net2 VN VN sky130_fd_pr__nfet_01v8_lvt L=0.3 W=2 nf=1 ad='int((nf+1)/2) * W/nf * 0.29' as='int((nf+2)/2) * W/nf * 0.29'
+ pd='2*int((nf+1)/2) * (W/nf + 0.29)' ps='2*int((nf+2)/2) * (W/nf + 0.29)' nrd='0.29 / W' nrs='0.29 / W'
+ sa=0 sb=0 sd=0 mult=34*6 m=34*6
XM4 OutP V_da2_N VM15D VN sky130_fd_pr__nfet_01v8_lvt L=0.15 W=2 nf=1 ad='int((nf+1)/2) * W/nf * 0.29'
+ as='int((nf+2)/2) * W/nf * 0.29' pd='2*int((nf+1)/2) * (W/nf + 0.29)' ps='2*int((nf+2)/2) * (W/nf + 0.29)'
+ nrd='0.29 / W' nrs='0.29 / W' sa=0 sb=0 sd=0 mult=30 m=30
XM23 V_da2_P InputSignal VM5D VN sky130_fd_pr__nfet_01v8_lvt L=0.15 W=2 nf=1 ad='int((nf+1)/2) * W/nf * 0.29'
+ as='int((nf+2)/2) * W/nf * 0.29' pd='2*int((nf+1)/2) * (W/nf + 0.29)' ps='2*int((nf+2)/2) * (W/nf + 0.29)'
+ nrd='0.29 / W' nrs='0.29 / W' sa=0 sb=0 sd=0 mult=6 m=6
XM19 OutN V_da2_P VM15D VN sky130_fd_pr__nfet_01v8_lvt L=0.15 W=2 nf=1 ad='int((nf+1)/2) * W/nf * 0.29'
+ as='int((nf+2)/2) * W/nf * 0.29' pd='2*int((nf+1)/2) * (W/nf + 0.29)' ps='2*int((nf+2)/2) * (W/nf + 0.29)'
+ nrd='0.29 / W' nrs='0.29 / W' sa=0 sb=0 sd=0 mult=30 m=30
XM14 V_da2_N InputRef VM5D VN sky130_fd_pr__nfet_01v8_lvt L=0.15 W=2 nf=1 ad='int((nf+1)/2) * W/nf * 0.29'
+ as='int((nf+2)/2) * W/nf * 0.29' pd='2*int((nf+1)/2) * (W/nf + 0.29)' ps='2*int((nf+2)/2) * (W/nf + 0.29)'
+ nrd='0.29 / W' nrs='0.29 / W' sa=0 sb=0 sd=0 mult=6 m=6
XR12 OutP VP VN sky130_fd_pr__res_high_po_1p41 L=4 mult=22 m=22
XR13 OutN VP VN sky130_fd_pr__res_high_po_1p41 L=4 mult=22 m=22
XR1 V_da2_P VP VN sky130_fd_pr__res_xhigh_po_1p41 L=2 mult=2*4 m=2*4
XR15 V_da2_N VP VN sky130_fd_pr__res_xhigh_po_1p41 L=2 mult=2*4 m=2*4
XC6 VN InputRef sky130_fd_pr__cap_mim_m3_1 W=10 L=6 MF=1 m=1
XC2 VN VP sky130_fd_pr__cap_mim_m3_1 W=15 L=30 MF=1 m=1
XC4 VN VP sky130_fd_pr__cap_mim_m3_1 W=15 L=30 MF=1 m=1
XC3 VN net2 sky130_fd_pr__cap_mim_m3_1 W=10 L=16 MF=1 m=1
.ends

.GLOBAL GND
.GLOBAL VDD
.end
